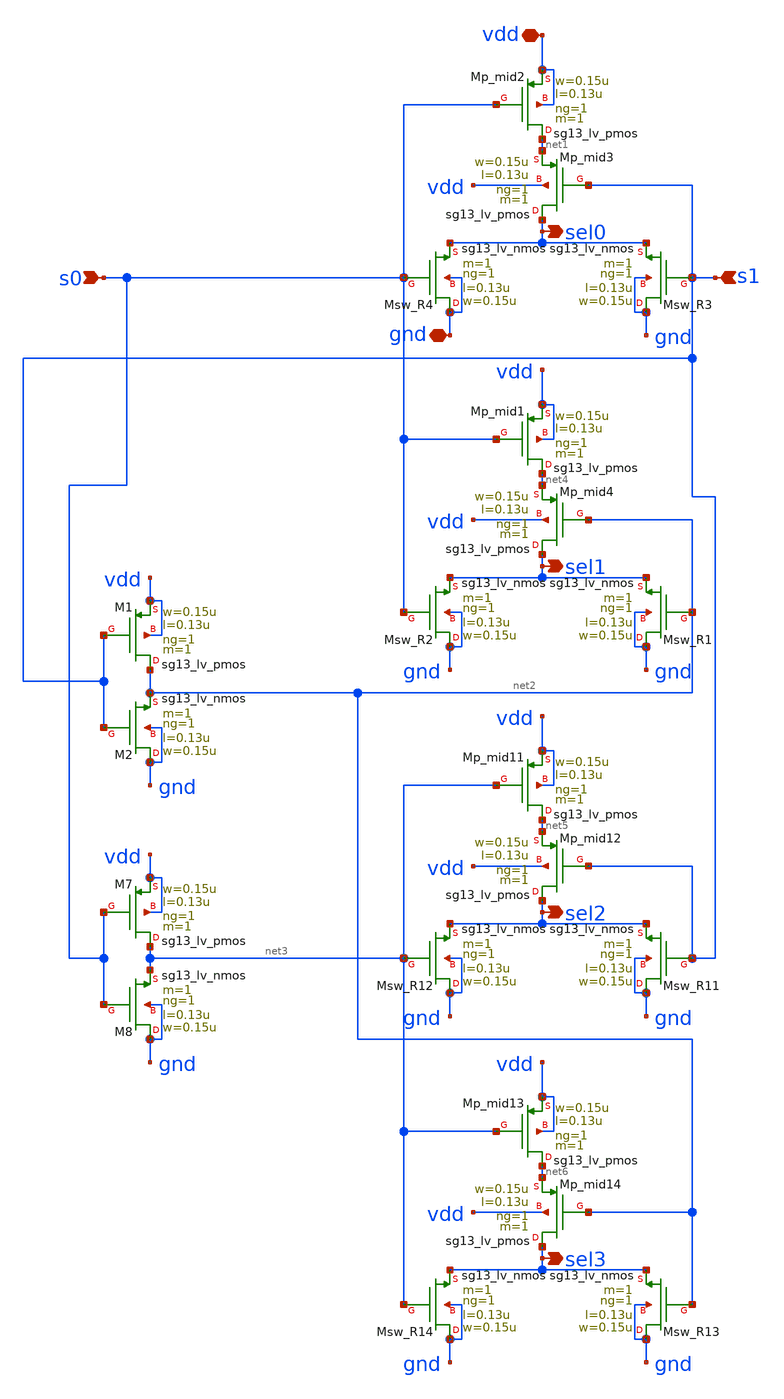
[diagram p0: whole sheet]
** sch_path: Enfoque_B/xschem/celdas/deco_2a4.sch
**.subckt deco_2a4 vdd gnd s0 s1 sel0 sel1 sel2 sel3
*.iopin vdd
*.iopin gnd
*.ipin s0
*.ipin s1
*.opin sel0
*.opin sel1
*.opin sel2
*.opin sel3
XMp_mid2 net1 s0 vdd vdd sg13_lv_pmos w=0.15u l=0.13u ng=1 m=1 mm_ok=1
XMp_mid3 sel0 s1 net1 vdd sg13_lv_pmos w=0.15u l=0.13u ng=1 m=1 mm_ok=1
XMsw_R3 gnd s1 sel0 gnd sg13_lv_nmos w=0.15u l=0.13u ng=1 m=1 mm_ok=1
XMsw_R4 gnd s0 sel0 gnd sg13_lv_nmos w=0.15u l=0.13u ng=1 m=1 mm_ok=1
XM1 net2 s1 vdd vdd sg13_lv_pmos w=0.15u l=0.13u ng=1 m=1 mm_ok=1
XM2 gnd s1 net2 gnd sg13_lv_nmos w=0.15u l=0.13u ng=1 m=1 mm_ok=1
XM7 net3 s0 vdd vdd sg13_lv_pmos w=0.15u l=0.13u ng=1 m=1 mm_ok=1
XM8 gnd s0 net3 gnd sg13_lv_nmos w=0.15u l=0.13u ng=1 m=1 mm_ok=1
XMp_mid1 net4 s0 vdd vdd sg13_lv_pmos w=0.15u l=0.13u ng=1 m=1 mm_ok=1
XMp_mid4 sel1 net2 net4 vdd sg13_lv_pmos w=0.15u l=0.13u ng=1 m=1 mm_ok=1
XMsw_R1 gnd net2 sel1 gnd sg13_lv_nmos w=0.15u l=0.13u ng=1 m=1 mm_ok=1
XMsw_R2 gnd s0 sel1 gnd sg13_lv_nmos w=0.15u l=0.13u ng=1 m=1 mm_ok=1
XMp_mid11 net5 net3 vdd vdd sg13_lv_pmos w=0.15u l=0.13u ng=1 m=1 mm_ok=1
XMp_mid12 sel2 s1 net5 vdd sg13_lv_pmos w=0.15u l=0.13u ng=1 m=1 mm_ok=1
XMsw_R11 gnd s1 sel2 gnd sg13_lv_nmos w=0.15u l=0.13u ng=1 m=1 mm_ok=1
XMsw_R12 gnd net3 sel2 gnd sg13_lv_nmos w=0.15u l=0.13u ng=1 m=1 mm_ok=1
XMp_mid13 net6 net3 vdd vdd sg13_lv_pmos w=0.15u l=0.13u ng=1 m=1 mm_ok=1
XMp_mid14 sel3 net2 net6 vdd sg13_lv_pmos w=0.15u l=0.13u ng=1 m=1 mm_ok=1
XMsw_R13 gnd net2 sel3 gnd sg13_lv_nmos w=0.15u l=0.13u ng=1 m=1 mm_ok=1
XMsw_R14 gnd net3 sel3 gnd sg13_lv_nmos w=0.15u l=0.13u ng=1 m=1 mm_ok=1
**.ends
.end
